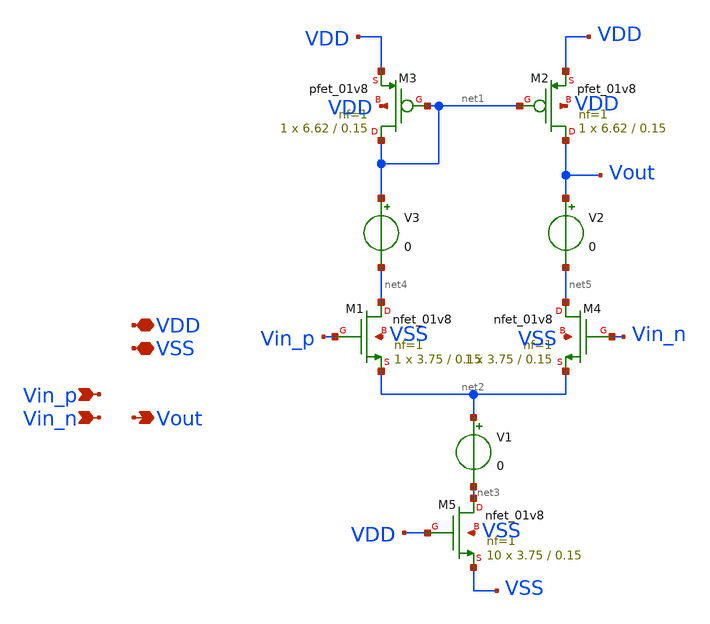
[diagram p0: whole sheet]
** sch_path: xschem/src/diff_to_se/diff_to_se.sch
**.subckt diff_to_se VDD Vout Vin_p Vin_n VSS
*.iopin VDD
*.opin Vout
*.ipin Vin_p
*.ipin Vin_n
*.iopin VSS
XM1 net4 Vin_p net2 VSS sky130_fd_pr__nfet_01v8 L=0.15 W=3.75 nf=1 ad='int((nf+1)/2) * W/nf * 0.29' as='int((nf+2)/2) * W/nf * 0.29'
+ pd='2*int((nf+1)/2) * (W/nf + 0.29)' ps='2*int((nf+2)/2) * (W/nf + 0.29)' nrd='0.29 / W' nrs='0.29 / W'
+ sa=0 sb=0 sd=0 mult=1 m=1
XM2 Vout net1 VDD VDD sky130_fd_pr__pfet_01v8 L=0.15 W=6.62 nf=1 ad='int((nf+1)/2) * W/nf * 0.29' as='int((nf+2)/2) * W/nf * 0.29'
+ pd='2*int((nf+1)/2) * (W/nf + 0.29)' ps='2*int((nf+2)/2) * (W/nf + 0.29)' nrd='0.29 / W' nrs='0.29 / W'
+ sa=0 sb=0 sd=0 mult=1 m=1
XM3 net1 net1 VDD VDD sky130_fd_pr__pfet_01v8 L=0.15 W=6.62 nf=1 ad='int((nf+1)/2) * W/nf * 0.29' as='int((nf+2)/2) * W/nf * 0.29'
+ pd='2*int((nf+1)/2) * (W/nf + 0.29)' ps='2*int((nf+2)/2) * (W/nf + 0.29)' nrd='0.29 / W' nrs='0.29 / W'
+ sa=0 sb=0 sd=0 mult=1 m=1
XM4 net5 Vin_n net2 VSS sky130_fd_pr__nfet_01v8 L=0.15 W=3.75 nf=1 ad='int((nf+1)/2) * W/nf * 0.29' as='int((nf+2)/2) * W/nf * 0.29'
+ pd='2*int((nf+1)/2) * (W/nf + 0.29)' ps='2*int((nf+2)/2) * (W/nf + 0.29)' nrd='0.29 / W' nrs='0.29 / W'
+ sa=0 sb=0 sd=0 mult=1 m=1
XM5 net3 VDD VSS VSS sky130_fd_pr__nfet_01v8 L=0.15 W=3.75 nf=1 ad='int((nf+1)/2) * W/nf * 0.29' as='int((nf+2)/2) * W/nf * 0.29'
+ pd='2*int((nf+1)/2) * (W/nf + 0.29)' ps='2*int((nf+2)/2) * (W/nf + 0.29)' nrd='0.29 / W' nrs='0.29 / W'
+ sa=0 sb=0 sd=0 mult=10 m=10
V1 net2 net3 0
V2 Vout net5 0
V3 net1 net4 0
**.ends
.end
